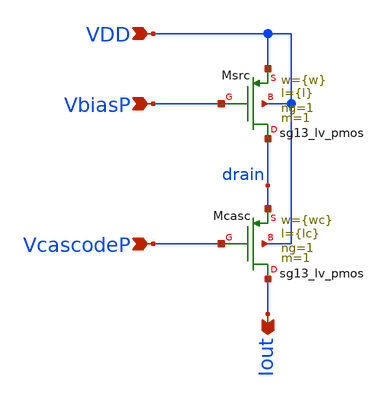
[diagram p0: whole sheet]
** sch_path: xschem/pcascsrc.sch
**.subckt pcascsrc VcascodeP VbiasP Iout VDD
*.ipin VcascodeP
*.ipin VbiasP
*.opin Iout
*.ipin VDD
XMsrc drain VbiasP VDD VDD sg13_lv_pmos w={w} l={l} ng=1 m=1 mm_ok=1
XMcasc Iout VcascodeP drain VDD sg13_lv_pmos w={wc} l={lc} ng=1 m=1 mm_ok=1
**.ends
.end
